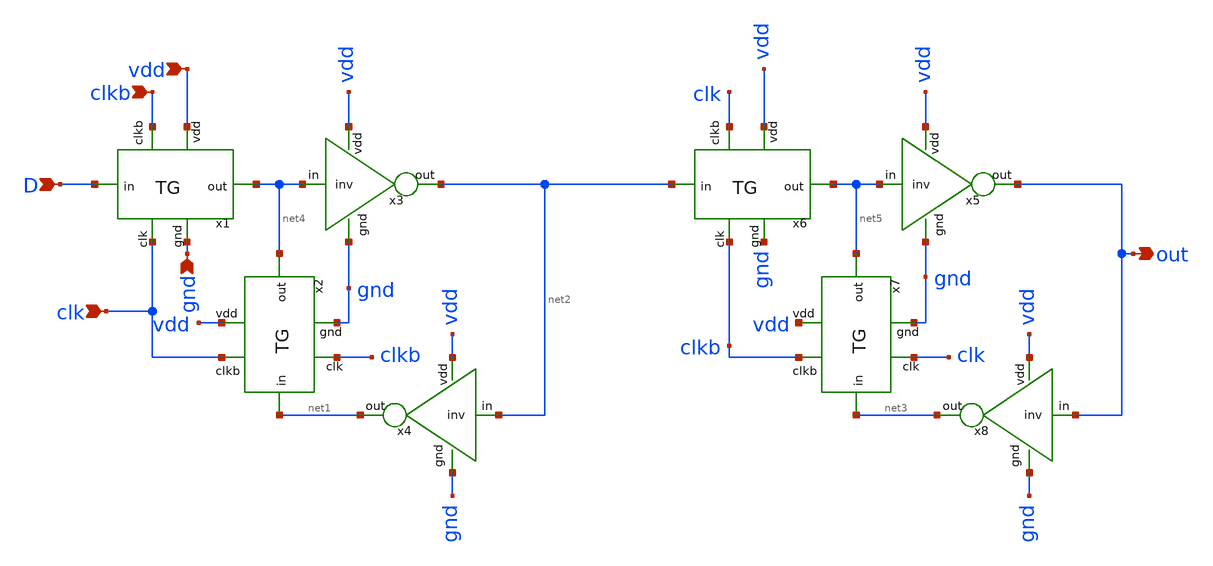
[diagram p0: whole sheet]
** sch_path: pll/dividers_lib/divider_init/xschem/DFF.sch
**.subckt DFF D clk clkb vdd gnd out
*.ipin D
*.ipin clk
*.ipin clkb
*.ipin vdd
*.ipin gnd
*.opin out
x3 vdd net4 net2 gnd inv
x1 clk vdd D net4 gnd clkb TG
x2 clkb vdd net1 net4 gnd clk TG
x4 vdd net2 net1 gnd inv
x5 vdd net5 out gnd inv
x6 clkb vdd net2 net5 gnd clk TG
x7 clk vdd net3 net5 gnd clkb TG
x8 vdd out net3 gnd inv
**.ends
.end
